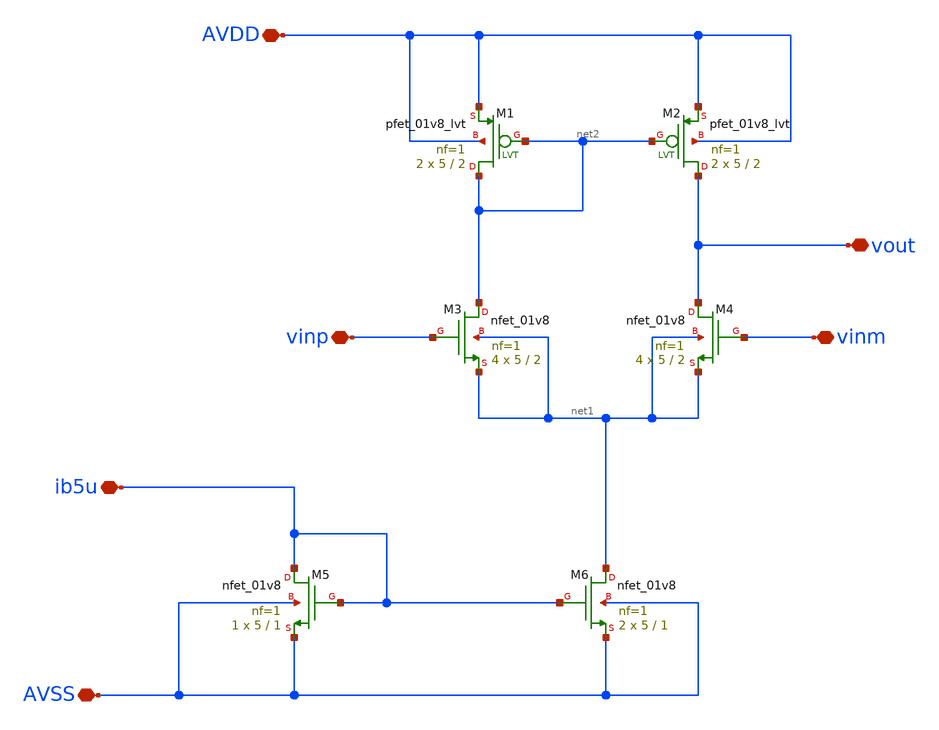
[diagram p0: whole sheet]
** sch_path: xschem/currentmirror1.sch
**.subckt currentmirror1 vinp vinm AVDD AVSS ib5u vout
*.iopin vinp
*.iopin vinm
*.iopin AVDD
*.iopin AVSS
*.iopin ib5u
*.iopin vout
XM5 ib5u ib5u AVSS AVSS sky130_fd_pr__nfet_01v8 L=1 W=5 nf=1 ad='int((1 + 1)/2) * 5 / 1 * 0.29' as='int((1 + 2)/2) * 5 / 1 * 0.29'
+ pd='2*int((1 + 1)/2) * (5 / 1 + 0.29)' ps='2*int((1 + 2)/2) * (5 / 1 + 0.29)' nrd='0.29 / 5 ' nrs='0.29 / 5 '
+ sa=0 sb=0 sd=0 mult=1 m=1
XM6 net1 ib5u AVSS AVSS sky130_fd_pr__nfet_01v8 L=1 W=5 nf=1 ad='int((1 + 1)/2) * 5 / 1 * 0.29' as='int((1 + 2)/2) * 5 / 1 * 0.29'
+ pd='2*int((1 + 1)/2) * (5 / 1 + 0.29)' ps='2*int((1 + 2)/2) * (5 / 1 + 0.29)' nrd='0.29 / 5 ' nrs='0.29 / 5 '
+ sa=0 sb=0 sd=0 mult=2 m=2
XM3 net2 vinp net1 net1 sky130_fd_pr__nfet_01v8 L=2 W=5 nf=1 ad='int((1 + 1)/2) * 5 / 1 * 0.29' as='int((1 + 2)/2) * 5 / 1 * 0.29'
+ pd='2*int((1 + 1)/2) * (5 / 1 + 0.29)' ps='2*int((1 + 2)/2) * (5 / 1 + 0.29)' nrd='0.29 / 5 ' nrs='0.29 / 5 '
+ sa=0 sb=0 sd=0 mult=4 m=4
XM4 vout vinm net1 net1 sky130_fd_pr__nfet_01v8 L=2 W=5 nf=1 ad='int((1 + 1)/2) * 5 / 1 * 0.29' as='int((1 + 2)/2) * 5 / 1 * 0.29'
+ pd='2*int((1 + 1)/2) * (5 / 1 + 0.29)' ps='2*int((1 + 2)/2) * (5 / 1 + 0.29)' nrd='0.29 / 5 ' nrs='0.29 / 5 '
+ sa=0 sb=0 sd=0 mult=4 m=4
XM1 net2 net2 AVDD AVDD sky130_fd_pr__pfet_01v8_lvt L=2 W=5 nf=1 ad='int((1 + 1)/2) * 5 / 1 * 0.29' as='int((1 + 2)/2) * 5 / 1 * 0.29'
+ pd='2*int((1 + 1)/2) * (5 / 1 + 0.29)' ps='2*int((1 + 2)/2) * (5 / 1 + 0.29)' nrd='0.29 / 5 ' nrs='0.29 / 5 '
+ sa=0 sb=0 sd=0 mult=2 m=2
XM2 vout net2 AVDD AVDD sky130_fd_pr__pfet_01v8_lvt L=2 W=5 nf=1 ad='int((1 + 1)/2) * 5 / 1 * 0.29' as='int((1 + 2)/2) * 5 / 1 * 0.29'
+ pd='2*int((1 + 1)/2) * (5 / 1 + 0.29)' ps='2*int((1 + 2)/2) * (5 / 1 + 0.29)' nrd='0.29 / 5 ' nrs='0.29 / 5 '
+ sa=0 sb=0 sd=0 mult=2 m=2
**.ends
.end
